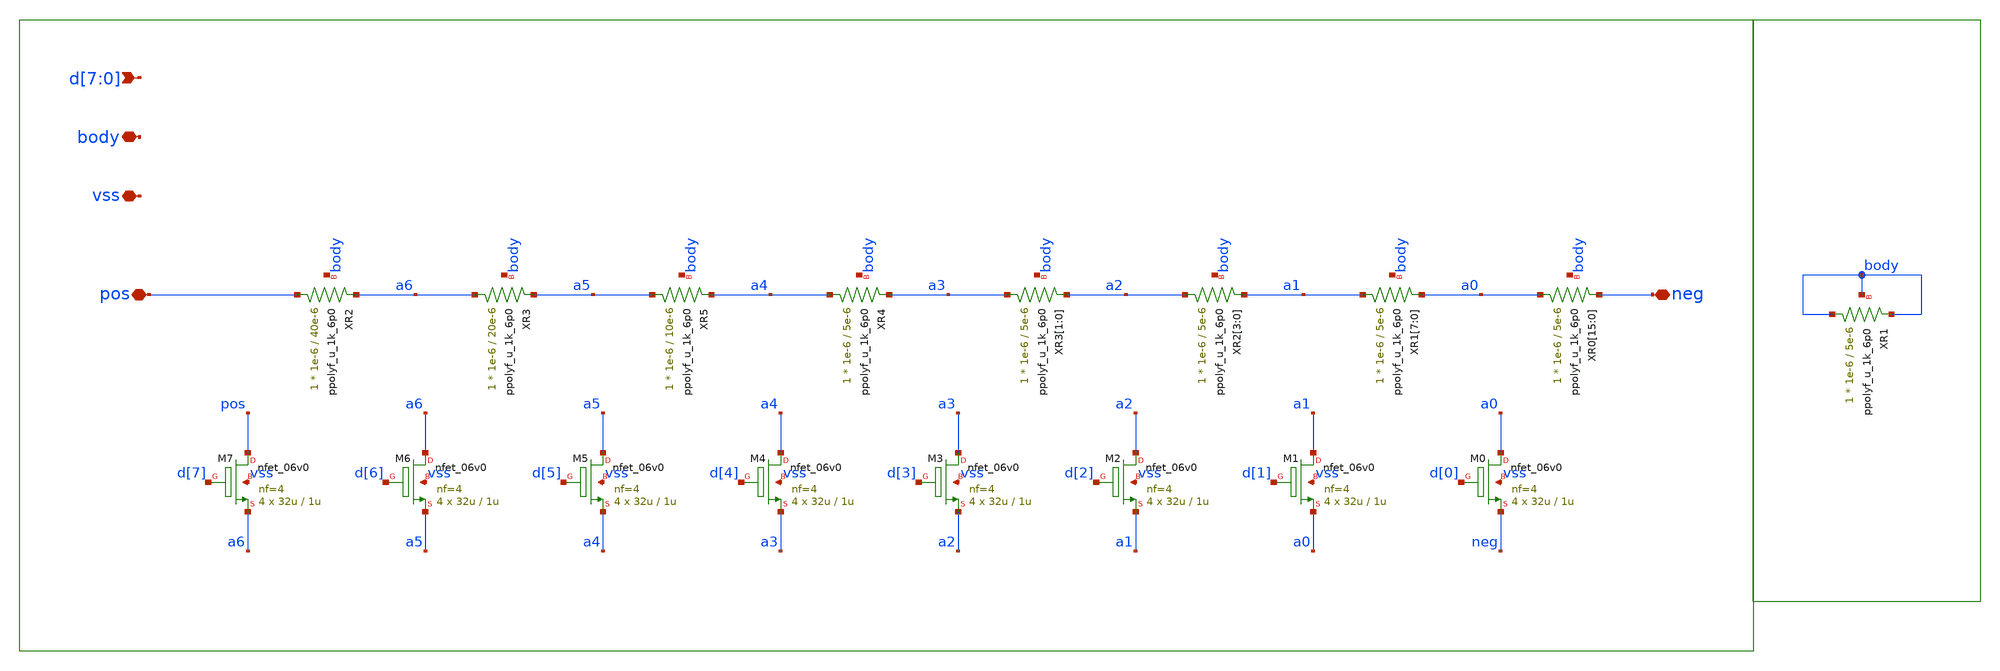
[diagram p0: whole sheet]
** sch_path: xschem/sch/bandgap_cm/bg_trimres/bg_trimres.sch
**.subckt bg_trimres d[7],d[6],d[5],d[4],d[3],d[2],d[1],d[0] pos neg vss body
*.ipin d[7],d[6],d[5],d[4],d[3],d[2],d[1],d[0]
*.iopin pos
*.iopin neg
*.iopin vss
*.iopin body
XM7 pos d[7] a6 vss nfet_06v0 L=1u W=32u nf=4 ad='int((nf+1)/2) * W/nf * 0.18u' as='int((nf+2)/2) * W/nf * 0.18u'
+ pd='2*int((nf+1)/2) * (W/nf + 0.18u)' ps='2*int((nf+2)/2) * (W/nf + 0.18u)' nrd='0.18u / W' nrs='0.18u / W'
+ sa=0 sb=0 sd=0 m=4 par=4
XM6 a6 d[6] a5 vss nfet_06v0 L=1u W=32u nf=4 ad='int((nf+1)/2) * W/nf * 0.18u' as='int((nf+2)/2) * W/nf * 0.18u'
+ pd='2*int((nf+1)/2) * (W/nf + 0.18u)' ps='2*int((nf+2)/2) * (W/nf + 0.18u)' nrd='0.18u / W' nrs='0.18u / W'
+ sa=0 sb=0 sd=0 m=4 par=4
XM5 a5 d[5] a4 vss nfet_06v0 L=1u W=32u nf=4 ad='int((nf+1)/2) * W/nf * 0.18u' as='int((nf+2)/2) * W/nf * 0.18u'
+ pd='2*int((nf+1)/2) * (W/nf + 0.18u)' ps='2*int((nf+2)/2) * (W/nf + 0.18u)' nrd='0.18u / W' nrs='0.18u / W'
+ sa=0 sb=0 sd=0 m=4 par=4
XM4 a4 d[4] a3 vss nfet_06v0 L=1u W=32u nf=4 ad='int((nf+1)/2) * W/nf * 0.18u' as='int((nf+2)/2) * W/nf * 0.18u'
+ pd='2*int((nf+1)/2) * (W/nf + 0.18u)' ps='2*int((nf+2)/2) * (W/nf + 0.18u)' nrd='0.18u / W' nrs='0.18u / W'
+ sa=0 sb=0 sd=0 m=4 par=4
XM3 a3 d[3] a2 vss nfet_06v0 L=1u W=32u nf=4 ad='int((nf+1)/2) * W/nf * 0.18u' as='int((nf+2)/2) * W/nf * 0.18u'
+ pd='2*int((nf+1)/2) * (W/nf + 0.18u)' ps='2*int((nf+2)/2) * (W/nf + 0.18u)' nrd='0.18u / W' nrs='0.18u / W'
+ sa=0 sb=0 sd=0 m=4 par=4
XR2 pos a6 body ppolyf_u_1k_6p0 r_width=1e-6 r_length=40e-6 s=1 m=1
XR3 a6 a5 body ppolyf_u_1k_6p0 r_width=1e-6 r_length=20e-6 s=1 m=1
XR5 a5 a4 body ppolyf_u_1k_6p0 r_width=1e-6 r_length=10e-6 s=1 m=1
XR4 a4 a3 body ppolyf_u_1k_6p0 r_width=1e-6 r_length=5e-6 s=1 m=1
XR3[1] a3 a2 body ppolyf_u_1k_6p0 r_width=1e-6 r_length=5e-6 s=1 m=1
XR3[0] a3 a2 body ppolyf_u_1k_6p0 r_width=1e-6 r_length=5e-6 s=1 m=1
XM2 a2 d[2] a1 vss nfet_06v0 L=1u W=32u nf=4 ad='int((nf+1)/2) * W/nf * 0.18u' as='int((nf+2)/2) * W/nf * 0.18u'
+ pd='2*int((nf+1)/2) * (W/nf + 0.18u)' ps='2*int((nf+2)/2) * (W/nf + 0.18u)' nrd='0.18u / W' nrs='0.18u / W'
+ sa=0 sb=0 sd=0 m=4 par=4
XR2[3] a2 a1 body ppolyf_u_1k_6p0 r_width=1e-6 r_length=5e-6 s=1 m=1
XR2[2] a2 a1 body ppolyf_u_1k_6p0 r_width=1e-6 r_length=5e-6 s=1 m=1
XR2[1] a2 a1 body ppolyf_u_1k_6p0 r_width=1e-6 r_length=5e-6 s=1 m=1
XR2[0] a2 a1 body ppolyf_u_1k_6p0 r_width=1e-6 r_length=5e-6 s=1 m=1
XR1[7] a1 a0 body ppolyf_u_1k_6p0 r_width=1e-6 r_length=5e-6 s=1 m=1
XR1[6] a1 a0 body ppolyf_u_1k_6p0 r_width=1e-6 r_length=5e-6 s=1 m=1
XR1[5] a1 a0 body ppolyf_u_1k_6p0 r_width=1e-6 r_length=5e-6 s=1 m=1
XR1[4] a1 a0 body ppolyf_u_1k_6p0 r_width=1e-6 r_length=5e-6 s=1 m=1
XR1[3] a1 a0 body ppolyf_u_1k_6p0 r_width=1e-6 r_length=5e-6 s=1 m=1
XR1[2] a1 a0 body ppolyf_u_1k_6p0 r_width=1e-6 r_length=5e-6 s=1 m=1
XR1[1] a1 a0 body ppolyf_u_1k_6p0 r_width=1e-6 r_length=5e-6 s=1 m=1
XR1[0] a1 a0 body ppolyf_u_1k_6p0 r_width=1e-6 r_length=5e-6 s=1 m=1
XM1 a1 d[1] a0 vss nfet_06v0 L=1u W=32u nf=4 ad='int((nf+1)/2) * W/nf * 0.18u' as='int((nf+2)/2) * W/nf * 0.18u'
+ pd='2*int((nf+1)/2) * (W/nf + 0.18u)' ps='2*int((nf+2)/2) * (W/nf + 0.18u)' nrd='0.18u / W' nrs='0.18u / W'
+ sa=0 sb=0 sd=0 m=4 par=4
XM0 a0 d[0] neg vss nfet_06v0 L=1u W=32u nf=4 ad='int((nf+1)/2) * W/nf * 0.18u' as='int((nf+2)/2) * W/nf * 0.18u'
+ pd='2*int((nf+1)/2) * (W/nf + 0.18u)' ps='2*int((nf+2)/2) * (W/nf + 0.18u)' nrd='0.18u / W' nrs='0.18u / W'
+ sa=0 sb=0 sd=0 m=4 par=4
XR0[15] a0 neg body ppolyf_u_1k_6p0 r_width=1e-6 r_length=5e-6 s=1 m=1
XR0[14] a0 neg body ppolyf_u_1k_6p0 r_width=1e-6 r_length=5e-6 s=1 m=1
XR0[13] a0 neg body ppolyf_u_1k_6p0 r_width=1e-6 r_length=5e-6 s=1 m=1
XR0[12] a0 neg body ppolyf_u_1k_6p0 r_width=1e-6 r_length=5e-6 s=1 m=1
XR0[11] a0 neg body ppolyf_u_1k_6p0 r_width=1e-6 r_length=5e-6 s=1 m=1
XR0[10] a0 neg body ppolyf_u_1k_6p0 r_width=1e-6 r_length=5e-6 s=1 m=1
XR0[9] a0 neg body ppolyf_u_1k_6p0 r_width=1e-6 r_length=5e-6 s=1 m=1
XR0[8] a0 neg body ppolyf_u_1k_6p0 r_width=1e-6 r_length=5e-6 s=1 m=1
XR0[7] a0 neg body ppolyf_u_1k_6p0 r_width=1e-6 r_length=5e-6 s=1 m=1
XR0[6] a0 neg body ppolyf_u_1k_6p0 r_width=1e-6 r_length=5e-6 s=1 m=1
XR0[5] a0 neg body ppolyf_u_1k_6p0 r_width=1e-6 r_length=5e-6 s=1 m=1
XR0[4] a0 neg body ppolyf_u_1k_6p0 r_width=1e-6 r_length=5e-6 s=1 m=1
XR0[3] a0 neg body ppolyf_u_1k_6p0 r_width=1e-6 r_length=5e-6 s=1 m=1
XR0[2] a0 neg body ppolyf_u_1k_6p0 r_width=1e-6 r_length=5e-6 s=1 m=1
XR0[1] a0 neg body ppolyf_u_1k_6p0 r_width=1e-6 r_length=5e-6 s=1 m=1
XR0[0] a0 neg body ppolyf_u_1k_6p0 r_width=1e-6 r_length=5e-6 s=1 m=1
XR1 body body body ppolyf_u_1k_6p0 r_width=1e-6 r_length=5e-6 s=1 m=5
**.ends
.end
